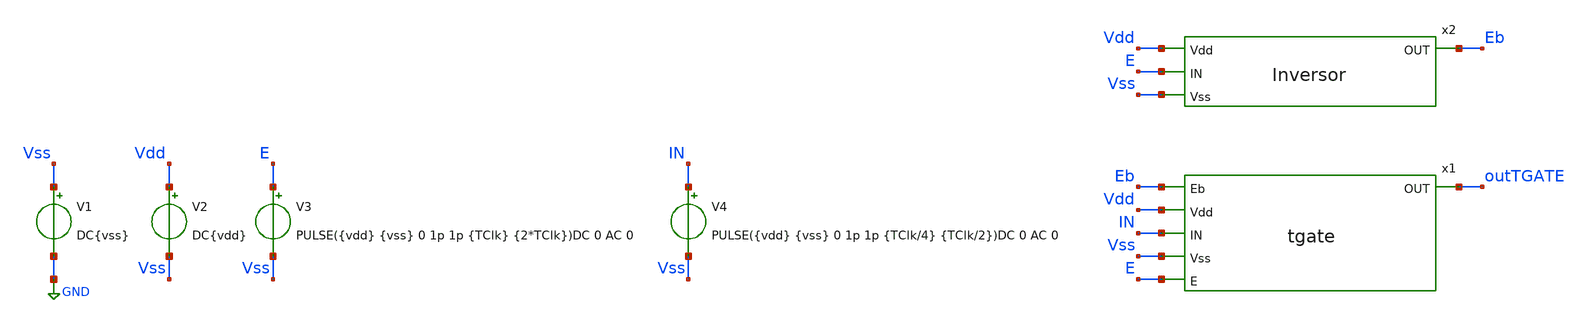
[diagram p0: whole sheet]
** sch_path: icdesign/sch/TGate/tb_tgate.sch
**.subckt tb_tgate
x1 Eb Vdd IN outTGATE Vss E tgate
V1 Vss GND DC{vss}
V2 Vdd Vss DC{vdd}
V3 E Vss PULSE({vdd} {vss} 0 1p 1p {TClk} {2*TClk})DC 0 AC 0
V4 IN Vss PULSE({vdd} {vss} 0 1p 1p {TClk/4} {TClk/2})DC 0 AC 0
x2 Vdd E Eb Vss Inversor
**** begin user architecture code





* Circuit Parameters
.param vdd  = 1.8
.param vss  = 0.0
.param Tclk = 10n
.options TEMP = 65.0


* Include Models
.lib ~/skywater/skywater-pdk/libraries/sky130_fd_pr_ngspice/latest/models/corners/sky130.lib TT


* OP Parameters & Singals to save
.save all


*Simulations
.control
  tran 0.01u 100n
  setplot tran1
  plot v(E)v(IN)+2 v(outTGATE)+4
.endc
.end


**** end user architecture code
**.ends

* expanding   symbol:  TGate/tgate.sym # of pins=6
** sym_path: icdesign/sch/TGate/tgate.sym
** sch_path: icdesign/sch/TGate/tgate.sch
.subckt tgate Eb Vdd IN OUT Vss E
*.opin OUT
*.ipin IN
*.ipin Eb
*.ipin E
*.ipin Vdd
*.ipin Vss
XM1 IN E OUT Vss sky130_fd_pr__nfet_01v8 L=0.15 W=0.75 nf=1 ad='int((nf+1)/2) * W/nf * 0.29' as='int((nf+2)/2) * W/nf * 0.29'
+ pd='2*int((nf+1)/2) * (W/nf + 0.29)' ps='2*int((nf+2)/2) * (W/nf + 0.29)' nrd='0.29 / W' nrs='0.29 / W'
+ sa=0 sb=0 sd=0 mult=1 m=1
XM2 IN Eb OUT Vdd sky130_fd_pr__pfet_01v8 L=0.15 W=0.75 nf=1 ad='int((nf+1)/2) * W/nf * 0.29' as='int((nf+2)/2) * W/nf * 0.29'
+ pd='2*int((nf+1)/2) * (W/nf + 0.29)' ps='2*int((nf+2)/2) * (W/nf + 0.29)' nrd='0.29 / W' nrs='0.29 / W'
+ sa=0 sb=0 sd=0 mult=2 m=2
.ends


* expanding   symbol:  Inversor/Inversor.sym # of pins=4
** sym_path: icdesign/sch/Inversor/Inversor.sym
** sch_path: icdesign/sch/Inversor/Inversor.sch
.subckt Inversor Vdd IN OUT Vss
*.ipin IN
*.ipin Vdd
*.ipin Vss
*.opin OUT
XM1 OUT IN Vss Vss sky130_fd_pr__nfet_01v8 L=0.15 W=0.75 nf=1 ad='int((nf+1)/2) * W/nf * 0.29' as='int((nf+2)/2) * W/nf * 0.29'
+ pd='2*int((nf+1)/2) * (W/nf + 0.29)' ps='2*int((nf+2)/2) * (W/nf + 0.29)' nrd='0.29 / W' nrs='0.29 / W'
+ sa=0 sb=0 sd=0 mult=1 m=1
XM2 OUT IN Vdd Vdd sky130_fd_pr__pfet_01v8 L=0.15 W=0.75 nf=1 ad='int((nf+1)/2) * W/nf * 0.29' as='int((nf+2)/2) * W/nf * 0.29'
+ pd='2*int((nf+1)/2) * (W/nf + 0.29)' ps='2*int((nf+2)/2) * (W/nf + 0.29)' nrd='0.29 / W' nrs='0.29 / W'
+ sa=0 sb=0 sd=0 mult=2 m=2
.ends

.GLOBAL GND
.end
